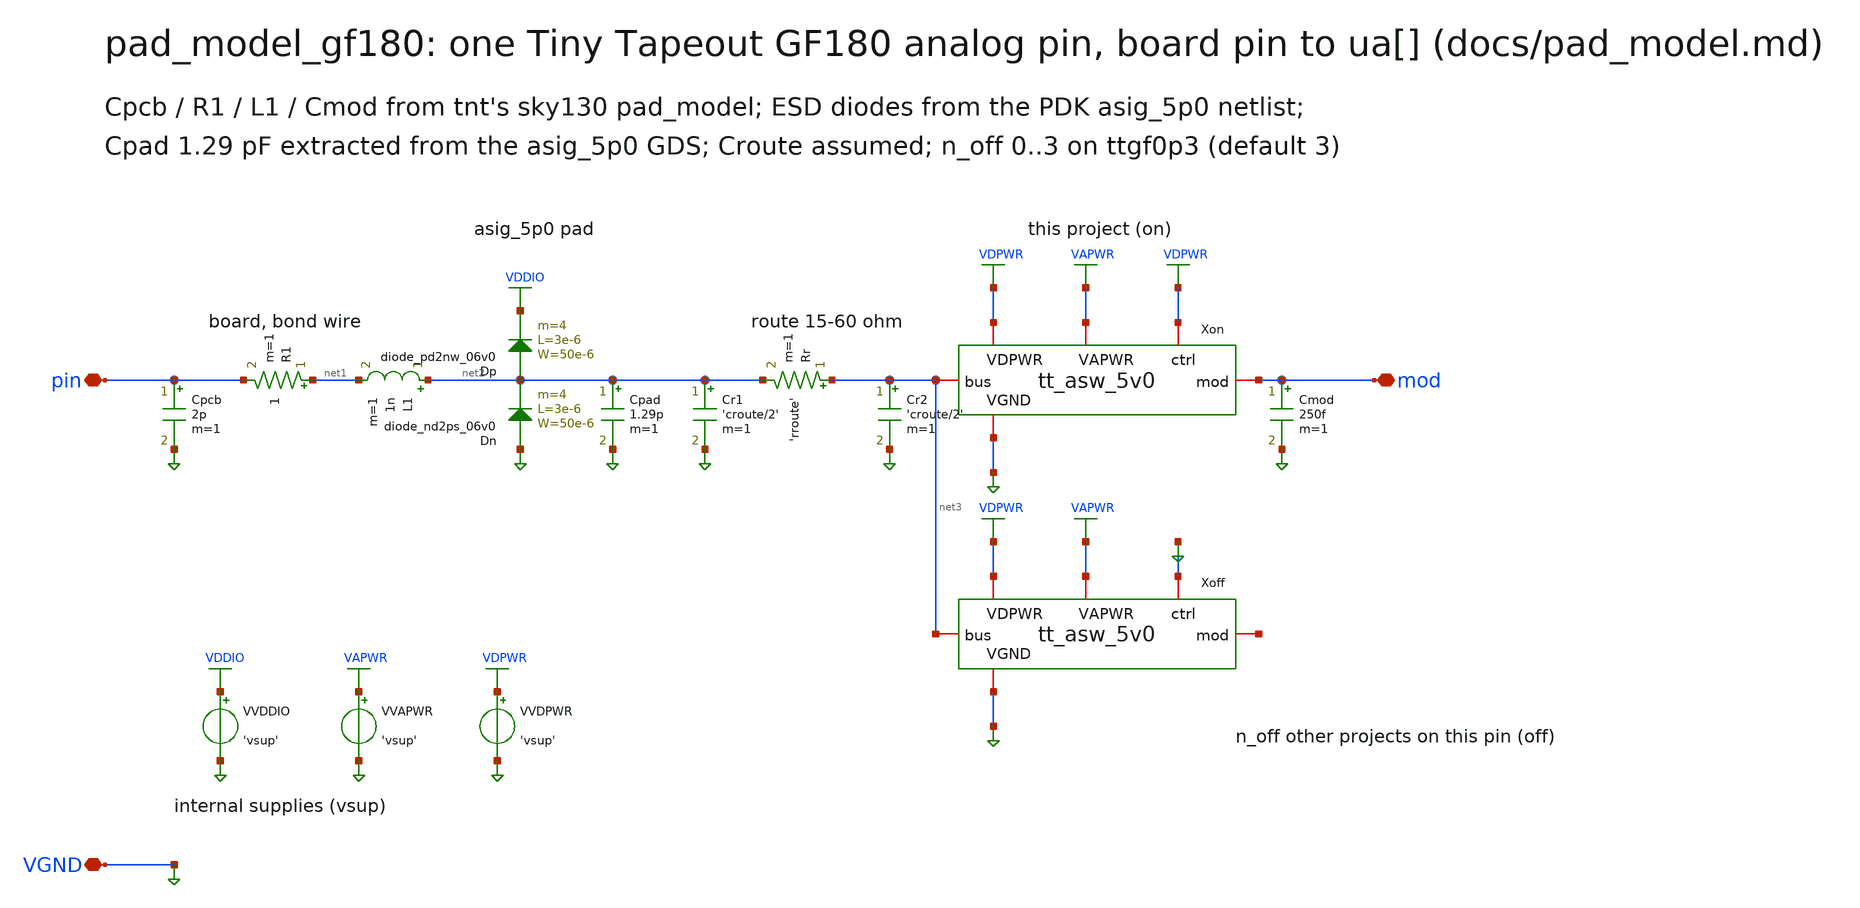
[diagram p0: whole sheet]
** sch_path: xschem/pad_model_gf180.sch
**.subckt pad_model_gf180 VGND pin mod
*.iopin VGND
*.iopin pin
*.iopin mod
Cpcb pin VGND 2p m=1
R1 net1 pin 1 m=1
L1 net2 net1 1n m=1
Dp net2 VDDIO diode_pd2nw_06v0 area='50e-6 * 3e-6 ' pj='2*50e-6 + 2*3e-6 ' m=4
Dn VGND net2 diode_nd2ps_06v0 area='50e-6 * 3e-6 ' pj='2*50e-6 + 2*3e-6 ' m=4
Cpad net2 VGND 1.29p m=1
Cr1 net2 VGND 'croute/2' m=1
Rr net3 net2 'rroute' m=1
Cr2 net3 VGND 'croute/2' m=1
Xon VGND VDPWR VAPWR VDPWR mod net3 tt_asw_5v0 mult=1
Cmod mod VGND 250f m=1
Xoff VGND VDPWR VAPWR VGND net4 net3 tt_asw_5v0 mult='max(n_off,1e-6)'
VVDDIO VDDIO VGND 'vsup'
VVAPWR VAPWR VGND 'vsup'
VVDPWR VDPWR VGND 'vsup'
**.ends

* expanding   symbol:  tt_asw_5v0.sym # of pins=6
** sym_path: xschem/tt_asw_5v0.sym
** sch_path: xschem/tt_asw_5v0.sch
.subckt tt_asw_5v0 VGND VDPWR VAPWR ctrl mod bus  mult=1
*.iopin VGND
*.iopin VDPWR
*.iopin VAPWR
*.ipin ctrl
*.iopin mod
*.iopin bus
x1 VGND VDPWR VAPWR ctrl net1 net2 lv2hv
XM2 bus net1 mod VGND nfet_05v0 L=0.6u W=31u nf=1 ad=3.189p as=3.189p pd=35.63u ps=35.63u nrd=0 nrs=0
+ sa=0 sb=0 sd=0 m='7*mult'
XM1 mod net2 bus VAPWR pfet_05v0 L=0.5u W=37u nf=1 ad=3.330p as=3.746p pd=37.18u ps=41.83u nrd=0 nrs=0
+ sa=0 sb=0 sd=0 m='16*mult'
XM3 mod net2 VGND VGND nfet_05v0 L=0.6u W=31u nf=1 ad=5.58p as=5.58p pd=62.36u ps=62.36u nrd=0 nrs=0
+ sa=0 sb=0 sd=0 m=mult
.ends


* expanding   symbol:  lv2hv.sym # of pins=6
** sym_path: xschem/lv2hv.sym
** sch_path: xschem/lv2hv.sch
.subckt lv2hv VGND VDPWR VAPWR in out_p out_n
*.iopin VGND
*.iopin VDPWR
*.iopin VAPWR
*.ipin in
*.opin out_p
*.opin out_n
XM1 net1 in VDPWR VDPWR pfet_03v3 L=0.28u W=2.0u nf=1 ad=0.36p as=0.36p pd=4.36u ps=4.36u nrd=0
+ nrs=0 sa=0 sb=0 sd=0 m=1
XM2 net1 in VGND VGND nfet_03v3 L=0.28u W=0.89u nf=1 ad=0.1602p as=0.1602p pd=2.14u ps=2.14u nrd=0
+ nrs=0 sa=0 sb=0 sd=0 m=1
XM3 net2 net1 VDPWR VDPWR pfet_03v3 L=0.28u W=2.0u nf=1 ad=0.36p as=0.36p pd=4.36u ps=4.36u nrd=0
+ nrs=0 sa=0 sb=0 sd=0 m=1
XM4 net2 net1 VGND VGND nfet_03v3 L=0.28u W=0.89u nf=1 ad=0.1602p as=0.1602p pd=2.14u ps=2.14u nrd=0
+ nrs=0 sa=0 sb=0 sd=0 m=1
XM5 net3 net4 VAPWR VAPWR pfet_05v0 L=0.5u W=0.5u nf=1 ad=0.09p as=0.09p pd=1.36u ps=1.36u nrd=0
+ nrs=0 sa=0 sb=0 sd=0 m=1
XM6 net3 net2 VGND VGND nfet_05v0 L=0.6u W=0.5u nf=1 ad=0.09p as=0.09p pd=1.36u ps=1.36u nrd=0 nrs=0
+ sa=0 sb=0 sd=0 m=1
XM7 net4 net3 VAPWR VAPWR pfet_05v0 L=0.5u W=0.5u nf=1 ad=0.09p as=0.09p pd=1.36u ps=1.36u nrd=0
+ nrs=0 sa=0 sb=0 sd=0 m=1
XM8 net4 net1 VGND VGND nfet_05v0 L=0.6u W=0.5u nf=1 ad=0.09p as=0.09p pd=1.36u ps=1.36u nrd=0 nrs=0
+ sa=0 sb=0 sd=0 m=1
XM9 out_p net3 VAPWR VAPWR pfet_05v0 L=0.5u W=1.0u nf=2 ad=0.09p as=0.18p pd=1.36u ps=2.72u nrd=0
+ nrs=0 sa=0 sb=0 sd=0 m=1
XM10 out_p net3 VGND VGND nfet_05v0 L=0.6u W=0.5u nf=1 ad=0.09p as=0.09p pd=1.36u ps=1.36u nrd=0
+ nrs=0 sa=0 sb=0 sd=0 m=1
XM11 out_n net4 VAPWR VAPWR pfet_05v0 L=0.5u W=1.0u nf=2 ad=0.09p as=0.18p pd=1.36u ps=2.72u nrd=0
+ nrs=0 sa=0 sb=0 sd=0 m=1
XM12 out_n net4 VGND VGND nfet_05v0 L=0.6u W=0.5u nf=1 ad=0.09p as=0.09p pd=1.36u ps=1.36u nrd=0
+ nrs=0 sa=0 sb=0 sd=0 m=1
.ends

.end
